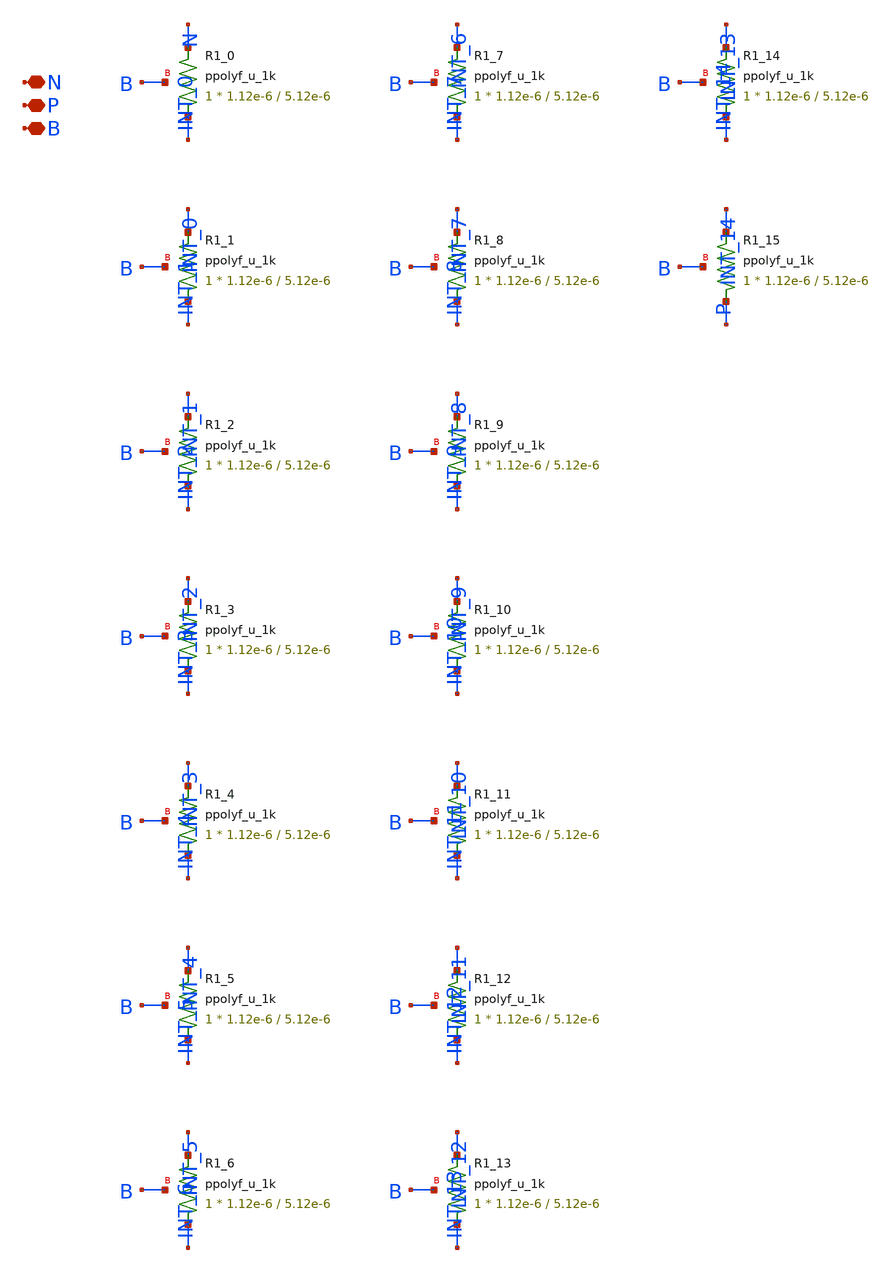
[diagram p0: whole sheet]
** sch_path: design/LELO_TR_GF180MCUD/LELOTR_RES16.sch
**.subckt LELOTR_RES16 N P B
*.iopin N
*.iopin P
*.iopin B
XR1_0 INT_0 N B ppolyf_u_1k r_width=1.12e-6 r_length=5.12e-6 m=1
XR1_1 INT_1 INT_0 B ppolyf_u_1k r_width=1.12e-6 r_length=5.12e-6 m=1
XR1_2 INT_2 INT_1 B ppolyf_u_1k r_width=1.12e-6 r_length=5.12e-6 m=1
XR1_3 INT_3 INT_2 B ppolyf_u_1k r_width=1.12e-6 r_length=5.12e-6 m=1
XR1_4 INT_4 INT_3 B ppolyf_u_1k r_width=1.12e-6 r_length=5.12e-6 m=1
XR1_5 INT_5 INT_4 B ppolyf_u_1k r_width=1.12e-6 r_length=5.12e-6 m=1
XR1_6 INT_6 INT_5 B ppolyf_u_1k r_width=1.12e-6 r_length=5.12e-6 m=1
XR1_7 INT_7 INT_6 B ppolyf_u_1k r_width=1.12e-6 r_length=5.12e-6 m=1
XR1_8 INT_8 INT_7 B ppolyf_u_1k r_width=1.12e-6 r_length=5.12e-6 m=1
XR1_9 INT_9 INT_8 B ppolyf_u_1k r_width=1.12e-6 r_length=5.12e-6 m=1
XR1_10 INT_10 INT_9 B ppolyf_u_1k r_width=1.12e-6 r_length=5.12e-6 m=1
XR1_11 INT_11 INT_10 B ppolyf_u_1k r_width=1.12e-6 r_length=5.12e-6 m=1
XR1_12 INT_12 INT_11 B ppolyf_u_1k r_width=1.12e-6 r_length=5.12e-6 m=1
XR1_13 INT_13 INT_12 B ppolyf_u_1k r_width=1.12e-6 r_length=5.12e-6 m=1
XR1_14 INT_14 INT_13 B ppolyf_u_1k r_width=1.12e-6 r_length=5.12e-6 m=1
XR1_15 P INT_14 B ppolyf_u_1k r_width=1.12e-6 r_length=5.12e-6 m=1
**.ends
.end
